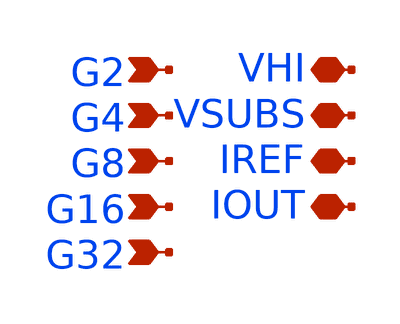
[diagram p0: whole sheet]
** sch_path: xschem/pmirror_tunable_64x_PEX.sch
**.subckt pmirror_tunable_64x_PEX G2 G4 G8 G16 G32 VHI VSUBS IREF IOUT
*.ipin G2
*.ipin G4
*.ipin G8
*.ipin G16
*.ipin G32
*.iopin VHI
*.iopin VSUBS
*.iopin IREF
*.iopin IOUT
**** begin user architecture code

* SPICE3 file created from pmirror_pfet_64x_complete.ext - technology: sky130B
X0 pmirror_pfet_64x_flat_0/G32 IREF VSUBS sky130_fd_pr__res_xhigh_po_0p35 l=500000u
X1 pmirror_pfet_64x_flat_0/G4  IREF VSUBS sky130_fd_pr__res_xhigh_po_0p35 l=500000u
X2 pmirror_pfet_64x_flat_0/G8  IREF VSUBS sky130_fd_pr__res_xhigh_po_0p35 l=500000u
X3 pmirror_pfet_64x_flat_0/G2  IREF VSUBS sky130_fd_pr__res_xhigh_po_0p35 l=500000u
X5 pmirror_pfet_64x_flat_0/G16 IREF VSUBS sky130_fd_pr__res_xhigh_po_0p35 l=500000u

X7 VHI pmirror_pfet_64x_flat_0/G32 IOUT VHI sky130_fd_pr__pfet_01v8 ad=0p pd=0u as=0p ps=0u w=1e+06u
+ l=300000u
X8 IOUT pmirror_pfet_64x_flat_0/G32 VHI VHI sky130_fd_pr__pfet_01v8 ad=0p pd=0u as=0p ps=0u w=1e+06u
+ l=300000u
X11 IOUT pmirror_pfet_64x_flat_0/G32 VHI VHI sky130_fd_pr__pfet_01v8 ad=0p pd=0u as=0p ps=0u
+ w=1e+06u l=300000u
X16 VHI pmirror_pfet_64x_flat_0/G32 IOUT VHI sky130_fd_pr__pfet_01v8 ad=0p pd=0u as=0p ps=0u
+ w=1e+06u l=300000u
X17 VHI pmirror_pfet_64x_flat_0/G32 IOUT VHI sky130_fd_pr__pfet_01v8 ad=0p pd=0u as=0p ps=0u
+ w=1e+06u l=300000u
X18 VHI pmirror_pfet_64x_flat_0/G32 IOUT VHI sky130_fd_pr__pfet_01v8 ad=0p pd=0u as=0p ps=0u
+ w=1e+06u l=300000u
X21 IOUT pmirror_pfet_64x_flat_0/G32 VHI VHI sky130_fd_pr__pfet_01v8 ad=0p pd=0u as=0p ps=0u
+ w=1e+06u l=300000u
X22 IOUT pmirror_pfet_64x_flat_0/G32 VHI VHI sky130_fd_pr__pfet_01v8 ad=0p pd=0u as=0p ps=0u
+ w=1e+06u l=300000u
X27 IOUT pmirror_pfet_64x_flat_0/G32 VHI VHI sky130_fd_pr__pfet_01v8 ad=1p pd=0u as=0p ps=0u
+ w=1e+06u l=300000u
X28 IOUT pmirror_pfet_64x_flat_0/G32 VHI VHI sky130_fd_pr__pfet_01v8 ad=0p pd=0u as=0p ps=0u
+ w=1e+06u l=300000u
X29 VHI pmirror_pfet_64x_flat_0/G32 IOUT VHI sky130_fd_pr__pfet_01v8 ad=0p pd=0u as=0p ps=0u
+ w=1e+06u l=300000u
X25 VHI pmirror_pfet_64x_flat_0/G32 IOUT VHI sky130_fd_pr__pfet_01v8 ad=0p pd=0u as=0p ps=0u
+ w=1e+06u l=300000u
X35 VHI pmirror_pfet_64x_flat_0/G32 IOUT VHI sky130_fd_pr__pfet_01v8 ad=0p pd=0u as=0p ps=0u
+ w=1e+06u l=300000u
X38 VHI pmirror_pfet_64x_flat_0/G32 IOUT VHI sky130_fd_pr__pfet_01v8 ad=0p pd=0u as=0p ps=0u
+ w=1e+06u l=300000u
X41 VHI pmirror_pfet_64x_flat_0/G32 IOUT VHI sky130_fd_pr__pfet_01v8 ad=0p pd=0u as=0p ps=0u
+ w=1e+06u l=300000u
X43 IOUT pmirror_pfet_64x_flat_0/G32 VHI VHI sky130_fd_pr__pfet_01v8 ad=0p pd=0u as=0p ps=0u
+ w=1e+06u l=300000u
X44 IOUT pmirror_pfet_64x_flat_0/G32 VHI VHI sky130_fd_pr__pfet_01v8 ad=0p pd=0u as=0p ps=0u
+ w=1e+06u l=300000u
X46 VHI pmirror_pfet_64x_flat_0/G32 IOUT VHI sky130_fd_pr__pfet_01v8 ad=0p pd=0u as=0p ps=0u
+ w=1e+06u l=300000u
X54 VHI pmirror_pfet_64x_flat_0/G32 IOUT VHI sky130_fd_pr__pfet_01v8 ad=0p pd=0u as=0p ps=0u
+ w=1e+06u l=300000u
X55 IOUT pmirror_pfet_64x_flat_0/G32 VHI VHI sky130_fd_pr__pfet_01v8 ad=0p pd=0u as=0p ps=0u
+ w=1e+06u l=300000u
X56 IOUT pmirror_pfet_64x_flat_0/G32 VHI VHI sky130_fd_pr__pfet_01v8 ad=0p pd=0u as=0p ps=0u
+ w=1e+06u l=300000u
X60 IOUT pmirror_pfet_64x_flat_0/G32 VHI VHI sky130_fd_pr__pfet_01v8 ad=0p pd=0u as=0p ps=0u
+ w=1e+06u l=300000u
X61 IOUT pmirror_pfet_64x_flat_0/G32 VHI VHI sky130_fd_pr__pfet_01v8 ad=0p pd=0u as=0p ps=0u
+ w=1e+06u l=300000u
X62 VHI pmirror_pfet_64x_flat_0/G32 IOUT VHI sky130_fd_pr__pfet_01v8 ad=0p pd=0u as=0p ps=0u
+ w=1e+06u l=300000u
X67 IOUT pmirror_pfet_64x_flat_0/G32 VHI VHI sky130_fd_pr__pfet_01v8 ad=0p pd=0u as=0p ps=0u
+ w=1e+06u l=300000u
X68 IOUT pmirror_pfet_64x_flat_0/G32 VHI VHI sky130_fd_pr__pfet_01v8 ad=0p pd=0u as=0p ps=0u
+ w=1e+06u l=300000u
X50 VHI pmirror_pfet_64x_flat_0/G32 IOUT VHI sky130_fd_pr__pfet_01v8 ad=0p pd=0u as=0p ps=0u
+ w=1e+06u l=300000u
X73 VHI pmirror_pfet_64x_flat_0/G32 IOUT VHI sky130_fd_pr__pfet_01v8 ad=0p pd=0u as=0p ps=0u
+ w=1e+06u l=300000u
X74 IOUT pmirror_pfet_64x_flat_0/G32 VHI VHI sky130_fd_pr__pfet_01v8 ad=0p pd=0u as=0p ps=0u
+ w=1e+06u l=300000u
X75 IOUT pmirror_pfet_64x_flat_0/G32 VHI VHI sky130_fd_pr__pfet_01v8 ad=0p pd=0u as=0p ps=0u
+ w=1e+06u l=300000u
X69 VHI pmirror_pfet_64x_flat_0/G32 IOUT VHI sky130_fd_pr__pfet_01v8 ad=0p pd=0u as=0p ps=0u
+ w=1e+06u l=300000u
X81 VHI pmirror_pfet_64x_flat_0/G32 IOUT VHI sky130_fd_pr__pfet_01v8 ad=0p pd=0u as=0p ps=0u
+ w=1e+06u l=300000u

X49 VHI VHI IOUT VHI sky130_fd_pr__pfet_01v8 ad=0p pd=0u as=0p ps=0u w=1e+06u l=300000u
X79 IREF IREF VHI VHI sky130_fd_pr__pfet_01v8 ad=0p pd=0u as=0p ps=0u w=1e+06u l=300000u

X6 IOUT pmirror_pfet_64x_flat_0/G16 VHI VHI sky130_fd_pr__pfet_01v8 ad=0p pd=0u as=0p ps=0u w=1e+06u
+ l=300000u
X9 VHI pmirror_pfet_64x_flat_0/G16 IOUT VHI sky130_fd_pr__pfet_01v8 ad=0p pd=0u as=0p ps=0u w=1e+06u
+ l=300000u
X10 IOUT pmirror_pfet_64x_flat_0/G16 VHI VHI sky130_fd_pr__pfet_01v8 ad=0p pd=0u as=0p ps=0u
+ w=1e+06u l=300000u
X19 IOUT pmirror_pfet_64x_flat_0/G16 VHI VHI sky130_fd_pr__pfet_01v8 ad=0p pd=0u as=0p ps=0u
+ w=1e+06u l=300000u
X20 IOUT pmirror_pfet_64x_flat_0/G16 VHI VHI sky130_fd_pr__pfet_01v8 ad=0p pd=0u as=0p ps=0u
+ w=1e+06u l=300000u
X26 VHI pmirror_pfet_64x_flat_0/G16 IOUT VHI sky130_fd_pr__pfet_01v8 ad=0p pd=0u as=0p ps=0u
+ w=1e+06u l=300000u
X30 IOUT pmirror_pfet_64x_flat_0/G16 VHI VHI sky130_fd_pr__pfet_01v8 ad=0p pd=0u as=0p ps=0u
+ w=1e+06u l=300000u
X33 IOUT pmirror_pfet_64x_flat_0/G16 VHI VHI sky130_fd_pr__pfet_01v8 ad=0p pd=0u as=0p ps=0u
+ w=1e+06u l=300000u
X36 VHI pmirror_pfet_64x_flat_0/G16 IOUT VHI sky130_fd_pr__pfet_01v8 ad=0p pd=0u as=0p ps=0u
+ w=1e+06u l=300000u
X45 VHI pmirror_pfet_64x_flat_0/G16 IOUT VHI sky130_fd_pr__pfet_01v8 ad=0p pd=0u as=0p ps=0u
+ w=1e+06u l=300000u
X53 VHI pmirror_pfet_64x_flat_0/G16 IOUT VHI sky130_fd_pr__pfet_01v8 ad=0p pd=0u as=0p ps=0u
+ w=1e+06u l=300000u
X57 VHI pmirror_pfet_64x_flat_0/G16 IOUT VHI sky130_fd_pr__pfet_01v8 ad=0p pd=0u as=0p ps=0u
+ w=1e+06u l=300000u
X58 VHI pmirror_pfet_64x_flat_0/G16 IOUT VHI sky130_fd_pr__pfet_01v8 ad=0p pd=0u as=0p ps=0u
+ w=1e+06u l=300000u
X65 VHI pmirror_pfet_64x_flat_0/G16 IOUT VHI sky130_fd_pr__pfet_01v8 ad=0p pd=0u as=0p ps=0u
+ w=1e+06u l=300000u
X82 IOUT pmirror_pfet_64x_flat_0/G16 VHI VHI sky130_fd_pr__pfet_01v8 ad=0p pd=0u as=0p ps=0u
+ w=1e+06u l=300000u
X83 IOUT pmirror_pfet_64x_flat_0/G16 VHI VHI sky130_fd_pr__pfet_01v8 ad=0p pd=0u as=0p ps=0u
+ w=1e+06u l=300000u

X14 IOUT pmirror_pfet_64x_flat_0/G8 VHI VHI sky130_fd_pr__pfet_01v8 ad=0p pd=0u as=0p ps=0u w=1e+06u
+ l=300000u
X23 VHI pmirror_pfet_64x_flat_0/G8 IOUT VHI sky130_fd_pr__pfet_01v8 ad=0p pd=0u as=0p ps=0u w=1e+06u
+ l=300000u
X31 VHI pmirror_pfet_64x_flat_0/G8 IOUT VHI sky130_fd_pr__pfet_01v8 ad=0p pd=0u as=0p ps=0u w=1e+06u
+ l=300000u
X32 VHI pmirror_pfet_64x_flat_0/G8 IOUT VHI sky130_fd_pr__pfet_01v8 ad=0p pd=0u as=0p ps=0u w=1e+06u
+ l=300000u
X42 VHI pmirror_pfet_64x_flat_0/G8 IOUT VHI sky130_fd_pr__pfet_01v8 ad=0p pd=0u as=0p ps=0u w=1e+06u
+ l=300000u
X72 IOUT pmirror_pfet_64x_flat_0/G8 VHI VHI sky130_fd_pr__pfet_01v8 ad=0p pd=0u as=0p ps=0u w=1e+06u
+ l=300000u
X80 IOUT pmirror_pfet_64x_flat_0/G8 VHI VHI sky130_fd_pr__pfet_01v8 ad=0p pd=0u as=0p ps=0u w=1e+06u
+ l=300000u
X84 IOUT pmirror_pfet_64x_flat_0/G8 VHI VHI sky130_fd_pr__pfet_01v8 ad=0p pd=0u as=0p ps=0u w=1e+06u
+ l=300000u

X85 IOUT pmirror_pfet_64x_flat_0/G4 VHI VHI sky130_fd_pr__pfet_01v8 ad=0p pd=0u as=0p ps=0u w=1e+06u
+ l=300000u
X39 VHI pmirror_pfet_64x_flat_0/G4 IOUT VHI sky130_fd_pr__pfet_01v8 ad=0p pd=0u as=0p ps=0u w=1e+06u
+ l=300000u
X40 VHI pmirror_pfet_64x_flat_0/G4 IOUT VHI sky130_fd_pr__pfet_01v8 ad=0p pd=0u as=0p ps=0u w=1e+06u
+ l=300000u
X70 IOUT pmirror_pfet_64x_flat_0/G4 VHI VHI sky130_fd_pr__pfet_01v8 ad=0p pd=0u as=0p ps=0u w=1e+06u
+ l=300000u

X48 VHI pmirror_pfet_64x_flat_0/G2 IOUT VHI sky130_fd_pr__pfet_01v8 ad=0p pd=0u as=0p ps=0u w=1e+06u
+ l=300000u
X15 IOUT pmirror_pfet_64x_flat_0/G2 VHI VHI sky130_fd_pr__pfet_01v8 ad=0p pd=0u as=0p ps=0u w=1e+06u
+ l=300000u

X86 VHI G32 pmirror_pfet_64x_flat_0/G32 VHI sky130_fd_pr__pfet_01v8 ad=0p pd=0u as=0p ps=0u
+ w=30e+06u l=150000u
X87 VHI G16 pmirror_pfet_64x_flat_0/G16 VHI sky130_fd_pr__pfet_01v8 ad=0p pd=0u as=0p ps=0u
+ w=30e+06u l=150000u
X88 VHI G2 pmirror_pfet_64x_flat_0/G2 VHI sky130_fd_pr__pfet_01v8 ad=0p pd=0u as=0p ps=0u w=30e+06u
+ l=150000u
X89 VHI G4 pmirror_pfet_64x_flat_0/G4 VHI sky130_fd_pr__pfet_01v8 ad=0p pd=0u as=0p ps=0u w=30e+06u
+ l=150000u
X90 VHI G8 pmirror_pfet_64x_flat_0/G8 VHI sky130_fd_pr__pfet_01v8 ad=0p pd=0u as=0p ps=0u w=30e+06u
+ l=150000u

C0 VHI pmirror_pfet_64x_flat_0/G8 10.15fF
C1 pmirror_pfet_64x_flat_0/G16 IOUT 2.36fF
C2 pmirror_pfet_64x_flat_0/G4 VHI 4.30fF
C3 pmirror_pfet_64x_flat_0/G2 IREF 2.13fF
C4 pmirror_pfet_64x_flat_0/G16 pmirror_pfet_64x_flat_0/G8 4.66fF
C5 pmirror_pfet_64x_flat_0/G4 pmirror_pfet_64x_flat_0/G8 3.24fF
C6 pmirror_pfet_64x_flat_0/G2 VHI 4.48fF
C7 pmirror_pfet_64x_flat_0/G4 pmirror_pfet_64x_flat_0/G2 2.55fF
C8 VHI IREF 4.53fF
C9 VHI pmirror_pfet_64x_flat_0/G32 15.40fF
C10 IOUT pmirror_pfet_64x_flat_0/G32 5.39fF
C11 pmirror_pfet_64x_flat_0/G16 pmirror_pfet_64x_flat_0/G32 3.74fF
C12 VHI IOUT 24.04fF
C13 pmirror_pfet_64x_flat_0/G16 VHI 4.93fF
C14 VHI VSUBS 46.10fF


**** end user architecture code
**.ends
.end
